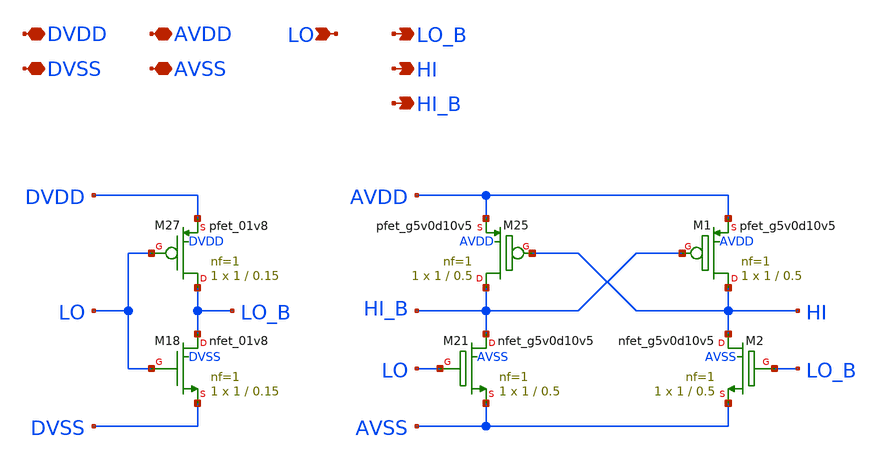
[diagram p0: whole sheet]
** sch_path: xschem/level_shifter.sch
**.subckt level_shifter DVDD DVSS AVDD AVSS LO LO_B HI HI_B
*.iopin DVDD
*.iopin DVSS
*.iopin AVDD
*.iopin AVSS
*.ipin LO
*.opin LO_B
*.opin HI
*.opin HI_B
XM18 LO_B LO DVSS DVSS sky130_fd_pr__nfet_01v8 L=0.15 W=1 nf=1 ad='int((nf+1)/2) * W/nf * 0.29' as='int((nf+2)/2) * W/nf * 0.29'
+ pd='2*int((nf+1)/2) * (W/nf + 0.29)' ps='2*int((nf+2)/2) * (W/nf + 0.29)' nrd='0.29 / W' nrs='0.29 / W'
+ sa=0 sb=0 sd=0 mult=1 m=1
XM21 HI_B LO AVSS AVSS sky130_fd_pr__nfet_g5v0d10v5 L=0.5 W=1 nf=1 ad='int((nf+1)/2) * W/nf * 0.29' as='int((nf+2)/2) * W/nf * 0.29'
+ pd='2*int((nf+1)/2) * (W/nf + 0.29)' ps='2*int((nf+2)/2) * (W/nf + 0.29)' nrd='0.29 / W' nrs='0.29 / W'
+ sa=0 sb=0 sd=0 mult=1 m=1
XM25 HI_B HI AVDD AVDD sky130_fd_pr__pfet_g5v0d10v5 L=0.5 W=1 nf=1 ad='int((nf+1)/2) * W/nf * 0.29' as='int((nf+2)/2) * W/nf * 0.29'
+ pd='2*int((nf+1)/2) * (W/nf + 0.29)' ps='2*int((nf+2)/2) * (W/nf + 0.29)' nrd='0.29 / W' nrs='0.29 / W'
+ sa=0 sb=0 sd=0 mult=1 m=1
XM27 LO_B LO DVDD DVDD sky130_fd_pr__pfet_01v8 L=0.15 W=1 nf=1 ad='int((1 + 1)/2) * 1 / 1 * 0.29' as='int((1 + 2)/2) * 1 / 1 * 0.29'
+ pd='2*int((1 + 1)/2) * (1 / 1 + 0.29)' ps='2*int((1 + 2)/2) * (1 / 1 + 0.29)' nrd='0.29 / 1 ' nrs='0.29 / 1 '
+ sa=0 sb=0 sd=0 mult=1 m=1
XM1 HI HI_B AVDD AVDD sky130_fd_pr__pfet_g5v0d10v5 L=0.5 W=1 nf=1 ad='int((nf+1)/2) * W/nf * 0.29' as='int((nf+2)/2) * W/nf * 0.29'
+ pd='2*int((nf+1)/2) * (W/nf + 0.29)' ps='2*int((nf+2)/2) * (W/nf + 0.29)' nrd='0.29 / W' nrs='0.29 / W'
+ sa=0 sb=0 sd=0 mult=1 m=1
XM2 HI LO_B AVSS AVSS sky130_fd_pr__nfet_g5v0d10v5 L=0.5 W=1 nf=1 ad='int((nf+1)/2) * W/nf * 0.29' as='int((nf+2)/2) * W/nf * 0.29'
+ pd='2*int((nf+1)/2) * (W/nf + 0.29)' ps='2*int((nf+2)/2) * (W/nf + 0.29)' nrd='0.29 / W' nrs='0.29 / W'
+ sa=0 sb=0 sd=0 mult=1 m=1
**.ends
.end
